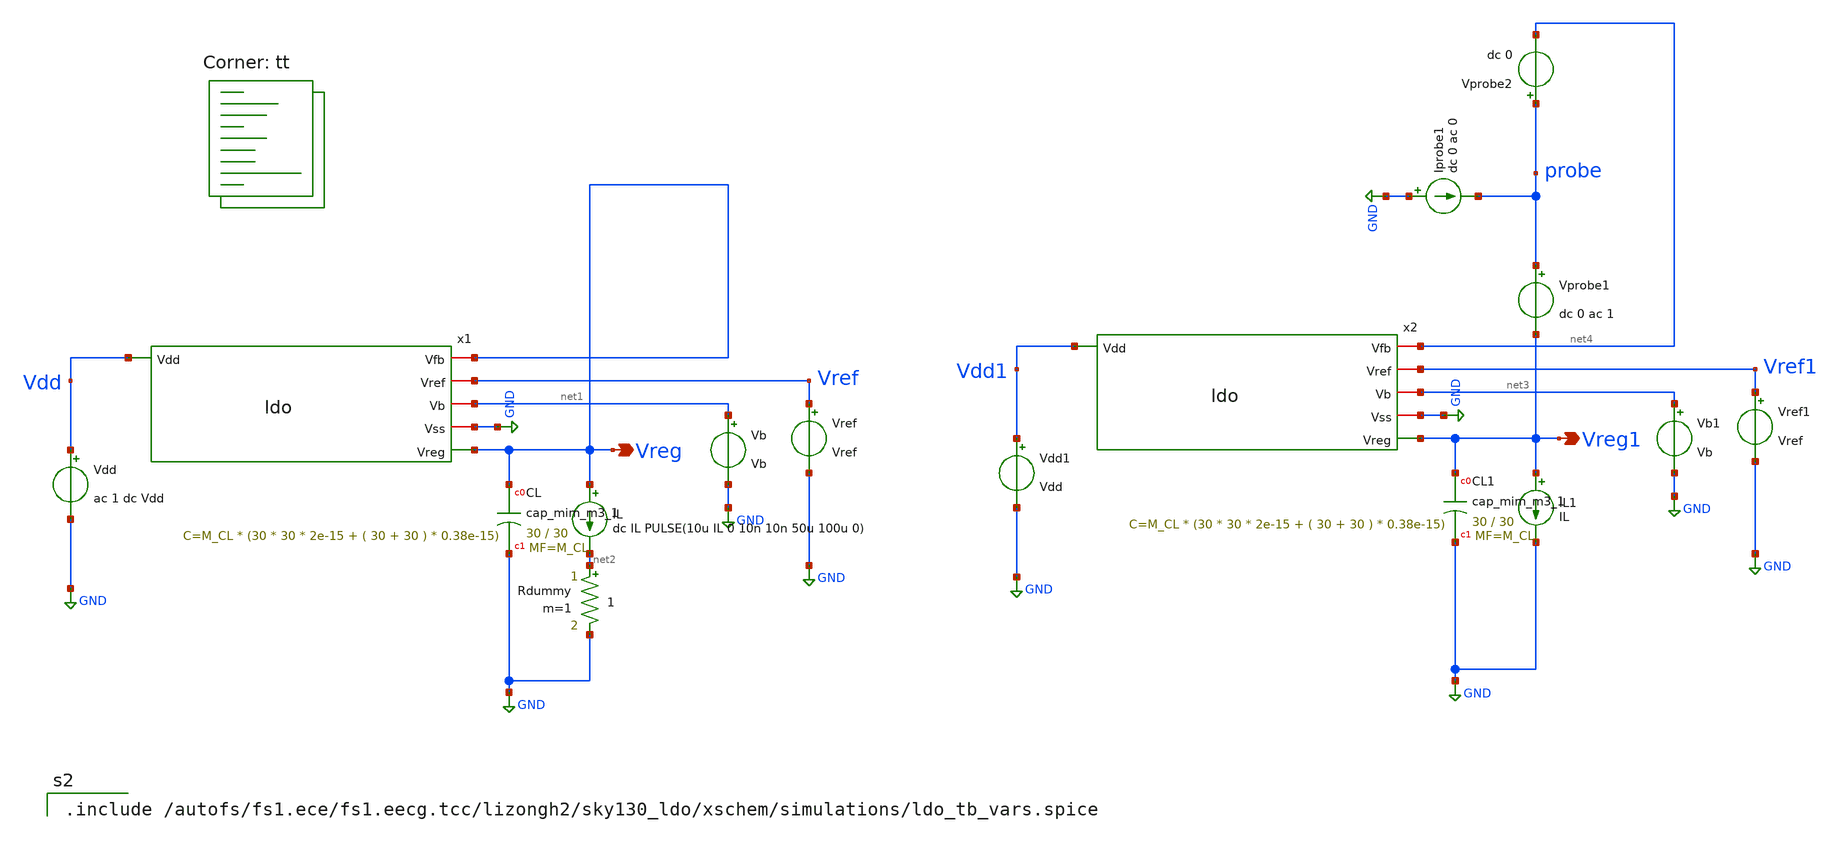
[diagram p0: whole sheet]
** sch_path: xschem/ldo_tb.sch
**.subckt ldo_tb Vreg Vreg1
*.opin Vreg
*.opin Vreg1
Vref Vref GND Vref
Vb net1 GND Vb
IL Vreg net2 dc IL PULSE(10u IL 0 10n 10n 50u 100u 0)
Vdd Vdd GND ac 1 dc Vdd
x1 Vdd Vreg Vref net1 GND Vreg ldo
XCL Vreg GND sky130_fd_pr__cap_mim_m3_1 W=30 L=30 MF=M_CL m=M_CL
Rdummy net2 GND 1 m=1
Vref1 Vref1 GND Vref
Vb1 net3 GND Vb
IL1 Vreg1 GND IL
Vdd1 Vdd1 GND Vdd
x2 Vdd1 net4 Vref1 net3 GND Vreg1 ldo
XCL1 Vreg1 GND sky130_fd_pr__cap_mim_m3_1 W=30 L=30 MF=M_CL m=M_CL
Vprobe2 probe net4 dc 0
Vprobe1 probe Vreg1 dc 0 ac 1
Iprobe1 GND probe dc 0 ac 0
**** begin user architecture code


*.OPTIONS maxord=1
.OPTIONS itl1=200
.OPTIONS itl2=200
.OPTIONS itl4=200

.control
* save all voltage and current
save all
.options savecurrents
set filetype=ascii
set units=degrees

* Loop stability
alter IL1 dc=10u
let runs=2
let run=0

alter @Vprobe1[acmag]=1
alter @Iprobe1[acmag]=0

dowhile run<runs
set run=$&run
set temp=27

ac dec 10 1 10G

alter @Vprobe1[acmag]=0
alter @Iprobe1[acmag]=1

let run=run+1
end

let ip11 = ac1.i(Vprobe1)
let ip12 = ac1.i(Vprobe2)
let ip21 = ac2.i(Vprobe1)
let ip22 = ac2.i(Vprobe2)
let vprb1 = ac1.v(probe)
let vprb2 = ac2.v(probe)

*** Middlebrook
let mb = 1/(vprb1+ip22)-1
*** Tian that is preferred
let av = 1/(1/(2*(ip11*vprb2-vprb1*ip21)+vprb1+ip21)-1)

plot vdb(mb) vp(mb)
plot vdb(av) vp(av)

wrdata ldo_tb_loop_gain_minload mag(av) vp(av)

* at max load
reset all
alter IL1 dc=10m
let runs=2
let run=0

alter @Vprobe1[acmag]=1
alter @Iprobe1[acmag]=0

dowhile run<runs
set run=$&run
set temp=27

ac dec 10 1 10G

alter @Vprobe1[acmag]=0
alter @Iprobe1[acmag]=1

let run=run+1
end

let ip11 = ac3.i(Vprobe1)
let ip12 = ac3.i(Vprobe2)
let ip21 = ac4.i(Vprobe1)
let ip22 = ac4.i(Vprobe2)
let vprb1 = ac3.v(probe)
let vprb2 = ac4.v(probe)

*** Middlebrook
let mb = 1/(vprb1+ip22)-1
*** Tian that is preferred
let av = 1/(1/(2*(ip11*vprb2-vprb1*ip21)+vprb1+ip21)-1)

plot vdb(mb) vp(mb)
plot vdb(av) vp(av)

wrdata ldo_tb_loop_gain_maxload mag(av) vp(av)

* DC sweep
dc Vdd 1 3 0.01
plot v(Vdd) v(Vreg)
wrdata ldo_tb_dc v(Vreg)

* Transient analysis with load regulation
* do not miss the space between the square bracket and number
tran 10n 100u
plot @Rdummy[i]
plot Vreg
wrdata ldo_tb_load_reg Vreg

* Transient analysis with line regulation
* at minimum load current 10uA
alter @IL[PULSE] [ 10u 10u 0 10n 10n 100u 100u 0 ]
alter @Vdd[PULSE] [ 2 3 0 1u 1u 25u 50u 0 ]
tran 10n 100u
plot Vdd
plot @Rdummy[i]
plot Vreg
wrdata ldo_tb_line_reg_minload Vreg

* at maximum load current 10mA
alter @IL[PULSE] [ 10m 10m 0 10n 10n 100u 100u 0 ]
tran 10n 100u
plot @Rdummy[i]
plot Vreg
wrdata ldo_tb_line_reg_maxload Vreg

* PSRR with max load
alter Vdd ac=1
alter Vprobe1 ac=0
ac dec 10 1 10G
plot vdb(Vreg)
wrdata ldo_tb_psrr_maxload mag(Vreg) vp(Vreg)

* PSRR with min load
alter IL dc=10u
ac dec 10 1 10G
plot vdb(Vreg)
wrdata ldo_tb_psrr_minload mag(Vreg) vp(Vreg)

* OP
op
let gmbs_M1=@m.x1.x1.XM1.msky130_fd_pr__nfet_g5v0d10v5[gmbs]
let gm_M1=@m.x1.x1.XM1.msky130_fd_pr__nfet_g5v0d10v5[gm]
let gds_M1=@m.x1.x1.XM1.msky130_fd_pr__nfet_g5v0d10v5[gds]
let vdsat_M1=@m.x1.x1.XM1.msky130_fd_pr__nfet_g5v0d10v5[vdsat]
let vth_M1=@m.x1.x1.XM1.msky130_fd_pr__nfet_g5v0d10v5[vth]
let id_M1=@m.x1.x1.XM1.msky130_fd_pr__nfet_g5v0d10v5[id]
let ibd_M1=@m.x1.x1.XM1.msky130_fd_pr__nfet_g5v0d10v5[ibd]
let ibs_M1=@m.x1.x1.XM1.msky130_fd_pr__nfet_g5v0d10v5[ibs]
let gbd_M1=@m.x1.x1.XM1.msky130_fd_pr__nfet_g5v0d10v5[gbd]
let gbs_M1=@m.x1.x1.XM1.msky130_fd_pr__nfet_g5v0d10v5[gbs]
let isub_M1=@m.x1.x1.XM1.msky130_fd_pr__nfet_g5v0d10v5[isub]
let igidl_M1=@m.x1.x1.XM1.msky130_fd_pr__nfet_g5v0d10v5[igidl]
let igisl_M1=@m.x1.x1.XM1.msky130_fd_pr__nfet_g5v0d10v5[igisl]
let igs_M1=@m.x1.x1.XM1.msky130_fd_pr__nfet_g5v0d10v5[igs]
let igd_M1=@m.x1.x1.XM1.msky130_fd_pr__nfet_g5v0d10v5[igd]
let igb_M1=@m.x1.x1.XM1.msky130_fd_pr__nfet_g5v0d10v5[igb]
let igcs_M1=@m.x1.x1.XM1.msky130_fd_pr__nfet_g5v0d10v5[igcs]
let vbs_M1=@m.x1.x1.XM1.msky130_fd_pr__nfet_g5v0d10v5[vbs]
let vgs_M1=@m.x1.x1.XM1.msky130_fd_pr__nfet_g5v0d10v5[vgs]
let vds_M1=@m.x1.x1.XM1.msky130_fd_pr__nfet_g5v0d10v5[vds]
let cgg_M1=@m.x1.x1.XM1.msky130_fd_pr__nfet_g5v0d10v5[cgg]
let cgs_M1=@m.x1.x1.XM1.msky130_fd_pr__nfet_g5v0d10v5[cgs]
let cgd_M1=@m.x1.x1.XM1.msky130_fd_pr__nfet_g5v0d10v5[cgd]
let cbg_M1=@m.x1.x1.XM1.msky130_fd_pr__nfet_g5v0d10v5[cbg]
let cbd_M1=@m.x1.x1.XM1.msky130_fd_pr__nfet_g5v0d10v5[cbd]
let cbs_M1=@m.x1.x1.XM1.msky130_fd_pr__nfet_g5v0d10v5[cbs]
let cdg_M1=@m.x1.x1.XM1.msky130_fd_pr__nfet_g5v0d10v5[cdg]
let cdd_M1=@m.x1.x1.XM1.msky130_fd_pr__nfet_g5v0d10v5[cdd]
let cds_M1=@m.x1.x1.XM1.msky130_fd_pr__nfet_g5v0d10v5[cds]
let csg_M1=@m.x1.x1.XM1.msky130_fd_pr__nfet_g5v0d10v5[csg]
let csd_M1=@m.x1.x1.XM1.msky130_fd_pr__nfet_g5v0d10v5[csd]
let css_M1=@m.x1.x1.XM1.msky130_fd_pr__nfet_g5v0d10v5[css]
let cgb_M1=@m.x1.x1.XM1.msky130_fd_pr__nfet_g5v0d10v5[cgb]
let cdb_M1=@m.x1.x1.XM1.msky130_fd_pr__nfet_g5v0d10v5[cdb]
let csb_M1=@m.x1.x1.XM1.msky130_fd_pr__nfet_g5v0d10v5[csb]
let cbb_M1=@m.x1.x1.XM1.msky130_fd_pr__nfet_g5v0d10v5[cbb]
let capbd_M1=@m.x1.x1.XM1.msky130_fd_pr__nfet_g5v0d10v5[capbd]
let capbs_M1=@m.x1.x1.XM1.msky130_fd_pr__nfet_g5v0d10v5[capbs]
let qg_M1=@m.x1.x1.XM1.msky130_fd_pr__nfet_g5v0d10v5[qg]
let qb_M1=@m.x1.x1.XM1.msky130_fd_pr__nfet_g5v0d10v5[qb]
let qs_M1=@m.x1.x1.XM1.msky130_fd_pr__nfet_g5v0d10v5[qs]
let qinv_M1=@m.x1.x1.XM1.msky130_fd_pr__nfet_g5v0d10v5[qinv]
let qdef_M1=@m.x1.x1.XM1.msky130_fd_pr__nfet_g5v0d10v5[qdef]
let gcrg_M1=@m.x1.x1.XM1.msky130_fd_pr__nfet_g5v0d10v5[gcrg]
let gtau_M1=@m.x1.x1.XM1.msky130_fd_pr__nfet_g5v0d10v5[gtau]

let gmbs_M2=@m.x1.x1.XM2.msky130_fd_pr__nfet_g5v0d10v5[gmbs]
let gm_M2=@m.x1.x1.XM2.msky130_fd_pr__nfet_g5v0d10v5[gm]
let gds_M2=@m.x1.x1.XM2.msky130_fd_pr__nfet_g5v0d10v5[gds]
let vdsat_M2=@m.x1.x1.XM2.msky130_fd_pr__nfet_g5v0d10v5[vdsat]
let vth_M2=@m.x1.x1.XM2.msky130_fd_pr__nfet_g5v0d10v5[vth]
let id_M2=@m.x1.x1.XM2.msky130_fd_pr__nfet_g5v0d10v5[id]
let ibd_M2=@m.x1.x1.XM2.msky130_fd_pr__nfet_g5v0d10v5[ibd]
let ibs_M2=@m.x1.x1.XM2.msky130_fd_pr__nfet_g5v0d10v5[ibs]
let gbd_M2=@m.x1.x1.XM2.msky130_fd_pr__nfet_g5v0d10v5[gbd]
let gbs_M2=@m.x1.x1.XM2.msky130_fd_pr__nfet_g5v0d10v5[gbs]
let isub_M2=@m.x1.x1.XM2.msky130_fd_pr__nfet_g5v0d10v5[isub]
let igidl_M2=@m.x1.x1.XM2.msky130_fd_pr__nfet_g5v0d10v5[igidl]
let igisl_M2=@m.x1.x1.XM2.msky130_fd_pr__nfet_g5v0d10v5[igisl]
let igs_M2=@m.x1.x1.XM2.msky130_fd_pr__nfet_g5v0d10v5[igs]
let igd_M2=@m.x1.x1.XM2.msky130_fd_pr__nfet_g5v0d10v5[igd]
let igb_M2=@m.x1.x1.XM2.msky130_fd_pr__nfet_g5v0d10v5[igb]
let igcs_M2=@m.x1.x1.XM2.msky130_fd_pr__nfet_g5v0d10v5[igcs]
let vbs_M2=@m.x1.x1.XM2.msky130_fd_pr__nfet_g5v0d10v5[vbs]
let vgs_M2=@m.x1.x1.XM2.msky130_fd_pr__nfet_g5v0d10v5[vgs]
let vds_M2=@m.x1.x1.XM2.msky130_fd_pr__nfet_g5v0d10v5[vds]
let cgg_M2=@m.x1.x1.XM2.msky130_fd_pr__nfet_g5v0d10v5[cgg]
let cgs_M2=@m.x1.x1.XM2.msky130_fd_pr__nfet_g5v0d10v5[cgs]
let cgd_M2=@m.x1.x1.XM2.msky130_fd_pr__nfet_g5v0d10v5[cgd]
let cbg_M2=@m.x1.x1.XM2.msky130_fd_pr__nfet_g5v0d10v5[cbg]
let cbd_M2=@m.x1.x1.XM2.msky130_fd_pr__nfet_g5v0d10v5[cbd]
let cbs_M2=@m.x1.x1.XM2.msky130_fd_pr__nfet_g5v0d10v5[cbs]
let cdg_M2=@m.x1.x1.XM2.msky130_fd_pr__nfet_g5v0d10v5[cdg]
let cdd_M2=@m.x1.x1.XM2.msky130_fd_pr__nfet_g5v0d10v5[cdd]
let cds_M2=@m.x1.x1.XM2.msky130_fd_pr__nfet_g5v0d10v5[cds]
let csg_M2=@m.x1.x1.XM2.msky130_fd_pr__nfet_g5v0d10v5[csg]
let csd_M2=@m.x1.x1.XM2.msky130_fd_pr__nfet_g5v0d10v5[csd]
let css_M2=@m.x1.x1.XM2.msky130_fd_pr__nfet_g5v0d10v5[css]
let cgb_M2=@m.x1.x1.XM2.msky130_fd_pr__nfet_g5v0d10v5[cgb]
let cdb_M2=@m.x1.x1.XM2.msky130_fd_pr__nfet_g5v0d10v5[cdb]
let csb_M2=@m.x1.x1.XM2.msky130_fd_pr__nfet_g5v0d10v5[csb]
let cbb_M2=@m.x1.x1.XM2.msky130_fd_pr__nfet_g5v0d10v5[cbb]
let capbd_M2=@m.x1.x1.XM2.msky130_fd_pr__nfet_g5v0d10v5[capbd]
let capbs_M2=@m.x1.x1.XM2.msky130_fd_pr__nfet_g5v0d10v5[capbs]
let qg_M2=@m.x1.x1.XM2.msky130_fd_pr__nfet_g5v0d10v5[qg]
let qb_M2=@m.x1.x1.XM2.msky130_fd_pr__nfet_g5v0d10v5[qb]
let qs_M2=@m.x1.x1.XM2.msky130_fd_pr__nfet_g5v0d10v5[qs]
let qinv_M2=@m.x1.x1.XM2.msky130_fd_pr__nfet_g5v0d10v5[qinv]
let qdef_M2=@m.x1.x1.XM2.msky130_fd_pr__nfet_g5v0d10v5[qdef]
let gcrg_M2=@m.x1.x1.XM2.msky130_fd_pr__nfet_g5v0d10v5[gcrg]
let gtau_M2=@m.x1.x1.XM2.msky130_fd_pr__nfet_g5v0d10v5[gtau]

let gmbs_M3=@m.x1.x1.XM3.msky130_fd_pr__pfet_g5v0d10v5[gmbs]
let gm_M3=@m.x1.x1.XM3.msky130_fd_pr__pfet_g5v0d10v5[gm]
let gds_M3=@m.x1.x1.XM3.msky130_fd_pr__pfet_g5v0d10v5[gds]
let vdsat_M3=@m.x1.x1.XM3.msky130_fd_pr__pfet_g5v0d10v5[vdsat]
let vth_M3=@m.x1.x1.XM3.msky130_fd_pr__pfet_g5v0d10v5[vth]
let id_M3=@m.x1.x1.XM3.msky130_fd_pr__pfet_g5v0d10v5[id]
let ibd_M3=@m.x1.x1.XM3.msky130_fd_pr__pfet_g5v0d10v5[ibd]
let ibs_M3=@m.x1.x1.XM3.msky130_fd_pr__pfet_g5v0d10v5[ibs]
let gbd_M3=@m.x1.x1.XM3.msky130_fd_pr__pfet_g5v0d10v5[gbd]
let gbs_M3=@m.x1.x1.XM3.msky130_fd_pr__pfet_g5v0d10v5[gbs]
let isub_M3=@m.x1.x1.XM3.msky130_fd_pr__pfet_g5v0d10v5[isub]
let igidl_M3=@m.x1.x1.XM3.msky130_fd_pr__pfet_g5v0d10v5[igidl]
let igisl_M3=@m.x1.x1.XM3.msky130_fd_pr__pfet_g5v0d10v5[igisl]
let igs_M3=@m.x1.x1.XM3.msky130_fd_pr__pfet_g5v0d10v5[igs]
let igd_M3=@m.x1.x1.XM3.msky130_fd_pr__pfet_g5v0d10v5[igd]
let igb_M3=@m.x1.x1.XM3.msky130_fd_pr__pfet_g5v0d10v5[igb]
let igcs_M3=@m.x1.x1.XM3.msky130_fd_pr__pfet_g5v0d10v5[igcs]
let vbs_M3=@m.x1.x1.XM3.msky130_fd_pr__pfet_g5v0d10v5[vbs]
let vgs_M3=@m.x1.x1.XM3.msky130_fd_pr__pfet_g5v0d10v5[vgs]
let vds_M3=@m.x1.x1.XM3.msky130_fd_pr__pfet_g5v0d10v5[vds]
let cgg_M3=@m.x1.x1.XM3.msky130_fd_pr__pfet_g5v0d10v5[cgg]
let cgs_M3=@m.x1.x1.XM3.msky130_fd_pr__pfet_g5v0d10v5[cgs]
let cgd_M3=@m.x1.x1.XM3.msky130_fd_pr__pfet_g5v0d10v5[cgd]
let cbg_M3=@m.x1.x1.XM3.msky130_fd_pr__pfet_g5v0d10v5[cbg]
let cbd_M3=@m.x1.x1.XM3.msky130_fd_pr__pfet_g5v0d10v5[cbd]
let cbs_M3=@m.x1.x1.XM3.msky130_fd_pr__pfet_g5v0d10v5[cbs]
let cdg_M3=@m.x1.x1.XM3.msky130_fd_pr__pfet_g5v0d10v5[cdg]
let cdd_M3=@m.x1.x1.XM3.msky130_fd_pr__pfet_g5v0d10v5[cdd]
let cds_M3=@m.x1.x1.XM3.msky130_fd_pr__pfet_g5v0d10v5[cds]
let csg_M3=@m.x1.x1.XM3.msky130_fd_pr__pfet_g5v0d10v5[csg]
let csd_M3=@m.x1.x1.XM3.msky130_fd_pr__pfet_g5v0d10v5[csd]
let css_M3=@m.x1.x1.XM3.msky130_fd_pr__pfet_g5v0d10v5[css]
let cgb_M3=@m.x1.x1.XM3.msky130_fd_pr__pfet_g5v0d10v5[cgb]
let cdb_M3=@m.x1.x1.XM3.msky130_fd_pr__pfet_g5v0d10v5[cdb]
let csb_M3=@m.x1.x1.XM3.msky130_fd_pr__pfet_g5v0d10v5[csb]
let cbb_M3=@m.x1.x1.XM3.msky130_fd_pr__pfet_g5v0d10v5[cbb]
let capbd_M3=@m.x1.x1.XM3.msky130_fd_pr__pfet_g5v0d10v5[capbd]
let capbs_M3=@m.x1.x1.XM3.msky130_fd_pr__pfet_g5v0d10v5[capbs]
let qg_M3=@m.x1.x1.XM3.msky130_fd_pr__pfet_g5v0d10v5[qg]
let qb_M3=@m.x1.x1.XM3.msky130_fd_pr__pfet_g5v0d10v5[qb]
let qs_M3=@m.x1.x1.XM3.msky130_fd_pr__pfet_g5v0d10v5[qs]
let qinv_M3=@m.x1.x1.XM3.msky130_fd_pr__pfet_g5v0d10v5[qinv]
let qdef_M3=@m.x1.x1.XM3.msky130_fd_pr__pfet_g5v0d10v5[qdef]
let gcrg_M3=@m.x1.x1.XM3.msky130_fd_pr__pfet_g5v0d10v5[gcrg]
let gtau_M3=@m.x1.x1.XM3.msky130_fd_pr__pfet_g5v0d10v5[gtau]

let gmbs_M4=@m.x1.x1.XM4.msky130_fd_pr__pfet_g5v0d10v5[gmbs]
let gm_M4=@m.x1.x1.XM4.msky130_fd_pr__pfet_g5v0d10v5[gm]
let gds_M4=@m.x1.x1.XM4.msky130_fd_pr__pfet_g5v0d10v5[gds]
let vdsat_M4=@m.x1.x1.XM4.msky130_fd_pr__pfet_g5v0d10v5[vdsat]
let vth_M4=@m.x1.x1.XM4.msky130_fd_pr__pfet_g5v0d10v5[vth]
let id_M4=@m.x1.x1.XM4.msky130_fd_pr__pfet_g5v0d10v5[id]
let ibd_M4=@m.x1.x1.XM4.msky130_fd_pr__pfet_g5v0d10v5[ibd]
let ibs_M4=@m.x1.x1.XM4.msky130_fd_pr__pfet_g5v0d10v5[ibs]
let gbd_M4=@m.x1.x1.XM4.msky130_fd_pr__pfet_g5v0d10v5[gbd]
let gbs_M4=@m.x1.x1.XM4.msky130_fd_pr__pfet_g5v0d10v5[gbs]
let isub_M4=@m.x1.x1.XM4.msky130_fd_pr__pfet_g5v0d10v5[isub]
let igidl_M4=@m.x1.x1.XM4.msky130_fd_pr__pfet_g5v0d10v5[igidl]
let igisl_M4=@m.x1.x1.XM4.msky130_fd_pr__pfet_g5v0d10v5[igisl]
let igs_M4=@m.x1.x1.XM4.msky130_fd_pr__pfet_g5v0d10v5[igs]
let igd_M4=@m.x1.x1.XM4.msky130_fd_pr__pfet_g5v0d10v5[igd]
let igb_M4=@m.x1.x1.XM4.msky130_fd_pr__pfet_g5v0d10v5[igb]
let igcs_M4=@m.x1.x1.XM4.msky130_fd_pr__pfet_g5v0d10v5[igcs]
let vbs_M4=@m.x1.x1.XM4.msky130_fd_pr__pfet_g5v0d10v5[vbs]
let vgs_M4=@m.x1.x1.XM4.msky130_fd_pr__pfet_g5v0d10v5[vgs]
let vds_M4=@m.x1.x1.XM4.msky130_fd_pr__pfet_g5v0d10v5[vds]
let cgg_M4=@m.x1.x1.XM4.msky130_fd_pr__pfet_g5v0d10v5[cgg]
let cgs_M4=@m.x1.x1.XM4.msky130_fd_pr__pfet_g5v0d10v5[cgs]
let cgd_M4=@m.x1.x1.XM4.msky130_fd_pr__pfet_g5v0d10v5[cgd]
let cbg_M4=@m.x1.x1.XM4.msky130_fd_pr__pfet_g5v0d10v5[cbg]
let cbd_M4=@m.x1.x1.XM4.msky130_fd_pr__pfet_g5v0d10v5[cbd]
let cbs_M4=@m.x1.x1.XM4.msky130_fd_pr__pfet_g5v0d10v5[cbs]
let cdg_M4=@m.x1.x1.XM4.msky130_fd_pr__pfet_g5v0d10v5[cdg]
let cdd_M4=@m.x1.x1.XM4.msky130_fd_pr__pfet_g5v0d10v5[cdd]
let cds_M4=@m.x1.x1.XM4.msky130_fd_pr__pfet_g5v0d10v5[cds]
let csg_M4=@m.x1.x1.XM4.msky130_fd_pr__pfet_g5v0d10v5[csg]
let csd_M4=@m.x1.x1.XM4.msky130_fd_pr__pfet_g5v0d10v5[csd]
let css_M4=@m.x1.x1.XM4.msky130_fd_pr__pfet_g5v0d10v5[css]
let cgb_M4=@m.x1.x1.XM4.msky130_fd_pr__pfet_g5v0d10v5[cgb]
let cdb_M4=@m.x1.x1.XM4.msky130_fd_pr__pfet_g5v0d10v5[cdb]
let csb_M4=@m.x1.x1.XM4.msky130_fd_pr__pfet_g5v0d10v5[csb]
let cbb_M4=@m.x1.x1.XM4.msky130_fd_pr__pfet_g5v0d10v5[cbb]
let capbd_M4=@m.x1.x1.XM4.msky130_fd_pr__pfet_g5v0d10v5[capbd]
let capbs_M4=@m.x1.x1.XM4.msky130_fd_pr__pfet_g5v0d10v5[capbs]
let qg_M4=@m.x1.x1.XM4.msky130_fd_pr__pfet_g5v0d10v5[qg]
let qb_M4=@m.x1.x1.XM4.msky130_fd_pr__pfet_g5v0d10v5[qb]
let qs_M4=@m.x1.x1.XM4.msky130_fd_pr__pfet_g5v0d10v5[qs]
let qinv_M4=@m.x1.x1.XM4.msky130_fd_pr__pfet_g5v0d10v5[qinv]
let qdef_M4=@m.x1.x1.XM4.msky130_fd_pr__pfet_g5v0d10v5[qdef]
let gcrg_M4=@m.x1.x1.XM4.msky130_fd_pr__pfet_g5v0d10v5[gcrg]
let gtau_M4=@m.x1.x1.XM4.msky130_fd_pr__pfet_g5v0d10v5[gtau]

let gmbs_M5=@m.x1.x1.XM5.msky130_fd_pr__nfet_g5v0d10v5[gmbs]
let gm_M5=@m.x1.x1.XM5.msky130_fd_pr__nfet_g5v0d10v5[gm]
let gds_M5=@m.x1.x1.XM5.msky130_fd_pr__nfet_g5v0d10v5[gds]
let vdsat_M5=@m.x1.x1.XM5.msky130_fd_pr__nfet_g5v0d10v5[vdsat]
let vth_M5=@m.x1.x1.XM5.msky130_fd_pr__nfet_g5v0d10v5[vth]
let id_M5=@m.x1.x1.XM5.msky130_fd_pr__nfet_g5v0d10v5[id]
let ibd_M5=@m.x1.x1.XM5.msky130_fd_pr__nfet_g5v0d10v5[ibd]
let ibs_M5=@m.x1.x1.XM5.msky130_fd_pr__nfet_g5v0d10v5[ibs]
let gbd_M5=@m.x1.x1.XM5.msky130_fd_pr__nfet_g5v0d10v5[gbd]
let gbs_M5=@m.x1.x1.XM5.msky130_fd_pr__nfet_g5v0d10v5[gbs]
let isub_M5=@m.x1.x1.XM5.msky130_fd_pr__nfet_g5v0d10v5[isub]
let igidl_M5=@m.x1.x1.XM5.msky130_fd_pr__nfet_g5v0d10v5[igidl]
let igisl_M5=@m.x1.x1.XM5.msky130_fd_pr__nfet_g5v0d10v5[igisl]
let igs_M5=@m.x1.x1.XM5.msky130_fd_pr__nfet_g5v0d10v5[igs]
let igd_M5=@m.x1.x1.XM5.msky130_fd_pr__nfet_g5v0d10v5[igd]
let igb_M5=@m.x1.x1.XM5.msky130_fd_pr__nfet_g5v0d10v5[igb]
let igcs_M5=@m.x1.x1.XM5.msky130_fd_pr__nfet_g5v0d10v5[igcs]
let vbs_M5=@m.x1.x1.XM5.msky130_fd_pr__nfet_g5v0d10v5[vbs]
let vgs_M5=@m.x1.x1.XM5.msky130_fd_pr__nfet_g5v0d10v5[vgs]
let vds_M5=@m.x1.x1.XM5.msky130_fd_pr__nfet_g5v0d10v5[vds]
let cgg_M5=@m.x1.x1.XM5.msky130_fd_pr__nfet_g5v0d10v5[cgg]
let cgs_M5=@m.x1.x1.XM5.msky130_fd_pr__nfet_g5v0d10v5[cgs]
let cgd_M5=@m.x1.x1.XM5.msky130_fd_pr__nfet_g5v0d10v5[cgd]
let cbg_M5=@m.x1.x1.XM5.msky130_fd_pr__nfet_g5v0d10v5[cbg]
let cbd_M5=@m.x1.x1.XM5.msky130_fd_pr__nfet_g5v0d10v5[cbd]
let cbs_M5=@m.x1.x1.XM5.msky130_fd_pr__nfet_g5v0d10v5[cbs]
let cdg_M5=@m.x1.x1.XM5.msky130_fd_pr__nfet_g5v0d10v5[cdg]
let cdd_M5=@m.x1.x1.XM5.msky130_fd_pr__nfet_g5v0d10v5[cdd]
let cds_M5=@m.x1.x1.XM5.msky130_fd_pr__nfet_g5v0d10v5[cds]
let csg_M5=@m.x1.x1.XM5.msky130_fd_pr__nfet_g5v0d10v5[csg]
let csd_M5=@m.x1.x1.XM5.msky130_fd_pr__nfet_g5v0d10v5[csd]
let css_M5=@m.x1.x1.XM5.msky130_fd_pr__nfet_g5v0d10v5[css]
let cgb_M5=@m.x1.x1.XM5.msky130_fd_pr__nfet_g5v0d10v5[cgb]
let cdb_M5=@m.x1.x1.XM5.msky130_fd_pr__nfet_g5v0d10v5[cdb]
let csb_M5=@m.x1.x1.XM5.msky130_fd_pr__nfet_g5v0d10v5[csb]
let cbb_M5=@m.x1.x1.XM5.msky130_fd_pr__nfet_g5v0d10v5[cbb]
let capbd_M5=@m.x1.x1.XM5.msky130_fd_pr__nfet_g5v0d10v5[capbd]
let capbs_M5=@m.x1.x1.XM5.msky130_fd_pr__nfet_g5v0d10v5[capbs]
let qg_M5=@m.x1.x1.XM5.msky130_fd_pr__nfet_g5v0d10v5[qg]
let qb_M5=@m.x1.x1.XM5.msky130_fd_pr__nfet_g5v0d10v5[qb]
let qs_M5=@m.x1.x1.XM5.msky130_fd_pr__nfet_g5v0d10v5[qs]
let qinv_M5=@m.x1.x1.XM5.msky130_fd_pr__nfet_g5v0d10v5[qinv]
let qdef_M5=@m.x1.x1.XM5.msky130_fd_pr__nfet_g5v0d10v5[qdef]
let gcrg_M5=@m.x1.x1.XM5.msky130_fd_pr__nfet_g5v0d10v5[gcrg]
let gtau_M5=@m.x1.x1.XM5.msky130_fd_pr__nfet_g5v0d10v5[gtau]

let gmbs_M6=@m.x1.XM6.msky130_fd_pr__pfet_g5v0d10v5[gmbs]
let gm_M6=@m.x1.XM6.msky130_fd_pr__pfet_g5v0d10v5[gm]
let gds_M6=@m.x1.XM6.msky130_fd_pr__pfet_g5v0d10v5[gds]
let vdsat_M6=@m.x1.XM6.msky130_fd_pr__pfet_g5v0d10v5[vdsat]
let vth_M6=@m.x1.XM6.msky130_fd_pr__pfet_g5v0d10v5[vth]
let id_M6=@m.x1.XM6.msky130_fd_pr__pfet_g5v0d10v5[id]
let ibd_M6=@m.x1.XM6.msky130_fd_pr__pfet_g5v0d10v5[ibd]
let ibs_M6=@m.x1.XM6.msky130_fd_pr__pfet_g5v0d10v5[ibs]
let gbd_M6=@m.x1.XM6.msky130_fd_pr__pfet_g5v0d10v5[gbd]
let gbs_M6=@m.x1.XM6.msky130_fd_pr__pfet_g5v0d10v5[gbs]
let isub_M6=@m.x1.XM6.msky130_fd_pr__pfet_g5v0d10v5[isub]
let igidl_M6=@m.x1.XM6.msky130_fd_pr__pfet_g5v0d10v5[igidl]
let igisl_M6=@m.x1.XM6.msky130_fd_pr__pfet_g5v0d10v5[igisl]
let igs_M6=@m.x1.XM6.msky130_fd_pr__pfet_g5v0d10v5[igs]
let igd_M6=@m.x1.XM6.msky130_fd_pr__pfet_g5v0d10v5[igd]
let igb_M6=@m.x1.XM6.msky130_fd_pr__pfet_g5v0d10v5[igb]
let igcs_M6=@m.x1.XM6.msky130_fd_pr__pfet_g5v0d10v5[igcs]
let vbs_M6=@m.x1.XM6.msky130_fd_pr__pfet_g5v0d10v5[vbs]
let vgs_M6=@m.x1.XM6.msky130_fd_pr__pfet_g5v0d10v5[vgs]
let vds_M6=@m.x1.XM6.msky130_fd_pr__pfet_g5v0d10v5[vds]
let cgg_M6=@m.x1.XM6.msky130_fd_pr__pfet_g5v0d10v5[cgg]
let cgs_M6=@m.x1.XM6.msky130_fd_pr__pfet_g5v0d10v5[cgs]
let cgd_M6=@m.x1.XM6.msky130_fd_pr__pfet_g5v0d10v5[cgd]
let cbg_M6=@m.x1.XM6.msky130_fd_pr__pfet_g5v0d10v5[cbg]
let cbd_M6=@m.x1.XM6.msky130_fd_pr__pfet_g5v0d10v5[cbd]
let cbs_M6=@m.x1.XM6.msky130_fd_pr__pfet_g5v0d10v5[cbs]
let cdg_M6=@m.x1.XM6.msky130_fd_pr__pfet_g5v0d10v5[cdg]
let cdd_M6=@m.x1.XM6.msky130_fd_pr__pfet_g5v0d10v5[cdd]
let cds_M6=@m.x1.XM6.msky130_fd_pr__pfet_g5v0d10v5[cds]
let csg_M6=@m.x1.XM6.msky130_fd_pr__pfet_g5v0d10v5[csg]
let csd_M6=@m.x1.XM6.msky130_fd_pr__pfet_g5v0d10v5[csd]
let css_M6=@m.x1.XM6.msky130_fd_pr__pfet_g5v0d10v5[css]
let cgb_M6=@m.x1.XM6.msky130_fd_pr__pfet_g5v0d10v5[cgb]
let cdb_M6=@m.x1.XM6.msky130_fd_pr__pfet_g5v0d10v5[cdb]
let csb_M6=@m.x1.XM6.msky130_fd_pr__pfet_g5v0d10v5[csb]
let cbb_M6=@m.x1.XM6.msky130_fd_pr__pfet_g5v0d10v5[cbb]
let capbd_M6=@m.x1.XM6.msky130_fd_pr__pfet_g5v0d10v5[capbd]
let capbs_M6=@m.x1.XM6.msky130_fd_pr__pfet_g5v0d10v5[capbs]
let qg_M6=@m.x1.XM6.msky130_fd_pr__pfet_g5v0d10v5[qg]
let qb_M6=@m.x1.XM6.msky130_fd_pr__pfet_g5v0d10v5[qb]
let qs_M6=@m.x1.XM6.msky130_fd_pr__pfet_g5v0d10v5[qs]
let qinv_M6=@m.x1.XM6.msky130_fd_pr__pfet_g5v0d10v5[qinv]
let qdef_M6=@m.x1.XM6.msky130_fd_pr__pfet_g5v0d10v5[qdef]
let gcrg_M6=@m.x1.XM6.msky130_fd_pr__pfet_g5v0d10v5[gcrg]
let gtau_M6=@m.x1.XM6.msky130_fd_pr__pfet_g5v0d10v5[gtau]

write ldo_tb_op gmbs_M1 gm_M1 gds_M1 vdsat_M1 vth_M1 id_M1 ibd_M1 ibs_M1 gbd_M1 gbs_M1 isub_M1
+ igidl_M1 igisl_M1 igs_M1 igd_M1 igb_M1 igcs_M1 vbs_M1 vgs_M1 vds_M1 cgg_M1 cgs_M1 cgd_M1 cbg_M1 cbd_M1
+ cbs_M1 cdg_M1 cdd_M1 cds_M1 csg_M1 csd_M1 css_M1 cgb_M1 cdb_M1 csb_M1 cbb_M1 capbd_M1 capbs_M1 qg_M1 qb_M1
+ qs_M1 qinv_M1 qdef_M1 gcrg_M1 gtau_M1 gmbs_M2 gm_M2 gds_M2 vdsat_M2 vth_M2 id_M2 ibd_M2 ibs_M2 gbd_M2
+ gbs_M2 isub_M2 igidl_M2 igisl_M2 igs_M2 igd_M2 igb_M2 igcs_M2 vbs_M2 vgs_M2 vds_M2 cgg_M2 cgs_M2 cgd_M2
+ cbg_M2 cbd_M2 cbs_M2 cdg_M2 cdd_M2 cds_M2 csg_M2 csd_M2 css_M2 cgb_M2 cdb_M2 csb_M2 cbb_M2 capbd_M2
+ capbs_M2 qg_M2 qb_M2 qs_M2 qinv_M2 qdef_M2 gcrg_M2 gtau_M2 gmbs_M3 gm_M3 gds_M3 vdsat_M3 vth_M3 id_M3 ibd_M3
+ ibs_M3 gbd_M3 gbs_M3 isub_M3 igidl_M3 igisl_M3 igs_M3 igd_M3 igb_M3 igcs_M3 vbs_M3 vgs_M3 vds_M3 cgg_M3
+ cgs_M3 cgd_M3 cbg_M3 cbd_M3 cbs_M3 cdg_M3 cdd_M3 cds_M3 csg_M3 csd_M3 css_M3 cgb_M3 cdb_M3 csb_M3 cbb_M3
+ capbd_M3 capbs_M3 qg_M3 qb_M3 qs_M3 qinv_M3 qdef_M3 gcrg_M3 gtau_M3 gmbs_M4 gm_M4 gds_M4 vdsat_M4 vth_M4
+ id_M4 ibd_M4 ibs_M4 gbd_M4 gbs_M4 isub_M4 igidl_M4 igisl_M4 igs_M4 igd_M4 igb_M4 igcs_M4 vbs_M4 vgs_M4
+ vds_M4 cgg_M4 cgs_M4 cgd_M4 cbg_M4 cbd_M4 cbs_M4 cdg_M4 cdd_M4 cds_M4 csg_M4 csd_M4 css_M4 cgb_M4 cdb_M4
+ csb_M4 cbb_M4 capbd_M4 capbs_M4 qg_M4 qb_M4 qs_M4 qinv_M4 qdef_M4 gcrg_M4 gtau_M4 gmbs_M5 gm_M5 gds_M5
+ vdsat_M5 vth_M5 id_M5 ibd_M5 ibs_M5 gbd_M5 gbs_M5 isub_M5 igidl_M5 igisl_M5 igs_M5 igd_M5 igb_M5 igcs_M5
+ vbs_M5 vgs_M5 vds_M5 cgg_M5 cgs_M5 cgd_M5 cbg_M5 cbd_M5 cbs_M5 cdg_M5 cdd_M5 cds_M5 csg_M5 csd_M5 css_M5
+ cgb_M5 cdb_M5 csb_M5 cbb_M5 capbd_M5 capbs_M5 qg_M5 qb_M5 qs_M5 qinv_M5 qdef_M5 gcrg_M5 gtau_M5 gmbs_M6
+ gm_M6 gds_M6 vdsat_M6 vth_M6 id_M6 ibd_M6 ibs_M6 gbd_M6 gbs_M6 isub_M6 igidl_M6 igisl_M6 igs_M6 igd_M6
+ igb_M6 igcs_M6 vbs_M6 vgs_M6 vds_M6 cgg_M6 cgs_M6 cgd_M6 cbg_M6 cbd_M6 cbs_M6 cdg_M6 cdd_M6 cds_M6 csg_M6
+ csd_M6 css_M6 cgb_M6 cdb_M6 csb_M6 cbb_M6 capbd_M6 capbs_M6 qg_M6 qb_M6 qs_M6 qinv_M6 qdef_M6 gcrg_M6
+ gtau_M6
.endc



.include /autofs/fs1.ece/fs1.eecg.tcc/lizongh2/sky130_ldo/xschem/simulations/ldo_tb_vars.spice


.lib $::SKYWATER_MODELS/sky130.lib.spice tt
**** end user architecture code
**.ends

* expanding   symbol:  ldo.sym # of pins=6
** sym_path: xschem/ldo.sym
** sch_path: xschem/ldo.sch
.subckt ldo Vdd Vfb Vref Vb Vss Vreg
*.iopin Vb
*.iopin Vss
*.opin Vreg
*.iopin Vref
*.ipin Vdd
*.iopin Vfb
x1 Vdd net1 Vfb Vref Vb Vss diff_pair
XM6 Vreg net1 Vdd Vdd sky130_fd_pr__pfet_g5v0d10v5 L=L_pass W=W_pass nf=Nf_pass ad='int((nf+1)/2) * W/nf * 0.29'
+ as='int((nf+2)/2) * W/nf * 0.29' pd='2*int((nf+1)/2) * (W/nf + 0.29)' ps='2*int((nf+2)/2) * (W/nf + 0.29)'
+ nrd='0.29 / W' nrs='0.29 / W' sa=0 sb=0 sd=0 mult=M_pass m=M_pass
XCfb net2 Vreg sky130_fd_pr__cap_mim_m3_1 W=10 L=10 MF=M_Cfb m=M_Cfb
XRfb net2 net1 Vss sky130_fd_pr__res_high_po_0p35 L=3 mult=M_Rfb m=M_Rfb
.ends


* expanding   symbol:  diff_pair.sym # of pins=6
** sym_path: xschem/diff_pair.sym
** sch_path: xschem/diff_pair.sch
.subckt diff_pair Vdd vout vinp vinm Vb Vss
*.iopin Vdd
*.ipin vinm
*.ipin vinp
*.iopin Vb
*.opin vout
*.iopin Vss
XM1 net1 vinp net2 Vss sky130_fd_pr__nfet_g5v0d10v5 L=L_M1 W=W_M1 nf=1 ad='int((nf+1)/2) * W/nf * 0.29'
+ as='int((nf+2)/2) * W/nf * 0.29' pd='2*int((nf+1)/2) * (W/nf + 0.29)' ps='2*int((nf+2)/2) * (W/nf + 0.29)'
+ nrd='0.29 / W' nrs='0.29 / W' sa=0 sb=0 sd=0 mult=1 m=1
XM2 vout vinm net2 Vss sky130_fd_pr__nfet_g5v0d10v5 L=L_M2 W=W_M2 nf=1 ad='int((nf+1)/2) * W/nf * 0.29'
+ as='int((nf+2)/2) * W/nf * 0.29' pd='2*int((nf+1)/2) * (W/nf + 0.29)' ps='2*int((nf+2)/2) * (W/nf + 0.29)'
+ nrd='0.29 / W' nrs='0.29 / W' sa=0 sb=0 sd=0 mult=1 m=1
XM3 vout net1 Vdd Vdd sky130_fd_pr__pfet_g5v0d10v5 L=L_M3 W=W_M3 nf=1 ad='int((nf+1)/2) * W/nf * 0.29'
+ as='int((nf+2)/2) * W/nf * 0.29' pd='2*int((nf+1)/2) * (W/nf + 0.29)' ps='2*int((nf+2)/2) * (W/nf + 0.29)'
+ nrd='0.29 / W' nrs='0.29 / W' sa=0 sb=0 sd=0 mult=1 m=1
XM4 net1 net1 Vdd Vdd sky130_fd_pr__pfet_g5v0d10v5 L=L_M4 W=W_M4 nf=1 ad='int((nf+1)/2) * W/nf * 0.29'
+ as='int((nf+2)/2) * W/nf * 0.29' pd='2*int((nf+1)/2) * (W/nf + 0.29)' ps='2*int((nf+2)/2) * (W/nf + 0.29)'
+ nrd='0.29 / W' nrs='0.29 / W' sa=0 sb=0 sd=0 mult=1 m=1
XM5 net2 Vb Vss Vss sky130_fd_pr__nfet_g5v0d10v5 L=L_M5 W=W_M5 nf=1 ad='int((nf+1)/2) * W/nf * 0.29'
+ as='int((nf+2)/2) * W/nf * 0.29' pd='2*int((nf+1)/2) * (W/nf + 0.29)' ps='2*int((nf+2)/2) * (W/nf + 0.29)'
+ nrd='0.29 / W' nrs='0.29 / W' sa=0 sb=0 sd=0 mult=1 m=1
.ends

.GLOBAL GND
.end
